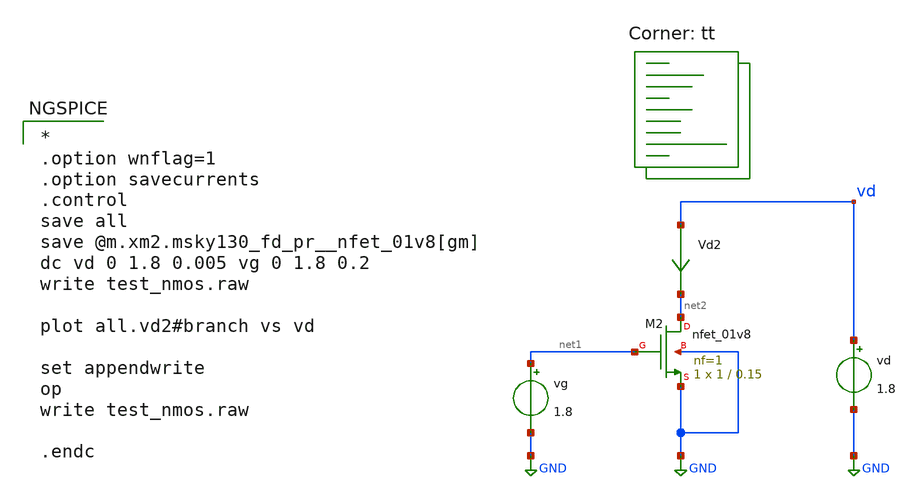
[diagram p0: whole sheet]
** sch_path: Modulo_Analogico/Lab1/dc_nfet_01v8.sch
**.subckt dc_nfet_01v8
Vd2 vd net2 0
.save i(vd2)
XM2 net2 net1 GND GND sky130_fd_pr__nfet_01v8 L=0.15 W=1 nf=1 ad='int((1 + 1)/2) * 1 / 1 * 0.29' as='int((1 + 2)/2) * 1 / 1 * 0.29'
+ pd='2*int((1 + 1)/2) * (1 / 1 + 0.29)' ps='2*int((1 + 2)/2) * (1 / 1 + 0.29)' nrd='0.29 / 1 ' nrs='0.29 / 1 '
+ sa=0 sb=0 sd=0 mult=1 m=1
vg net1 GND 1.8
vd vd GND 1.8
**** begin user architecture code

*
.option wnflag=1
.option savecurrents
.control
save all
save @m.xm2.msky130_fd_pr__nfet_01v8[gm]
dc vd 0 1.8 0.005 vg 0 1.8 0.2
write test_nmos.raw

plot all.vd2#branch vs vd

set appendwrite
op
write test_nmos.raw

.endc


.lib $::SKYWATER_MODELS/sky130.lib.spice tt
**** end user architecture code
**.ends
.GLOBAL GND
.end
